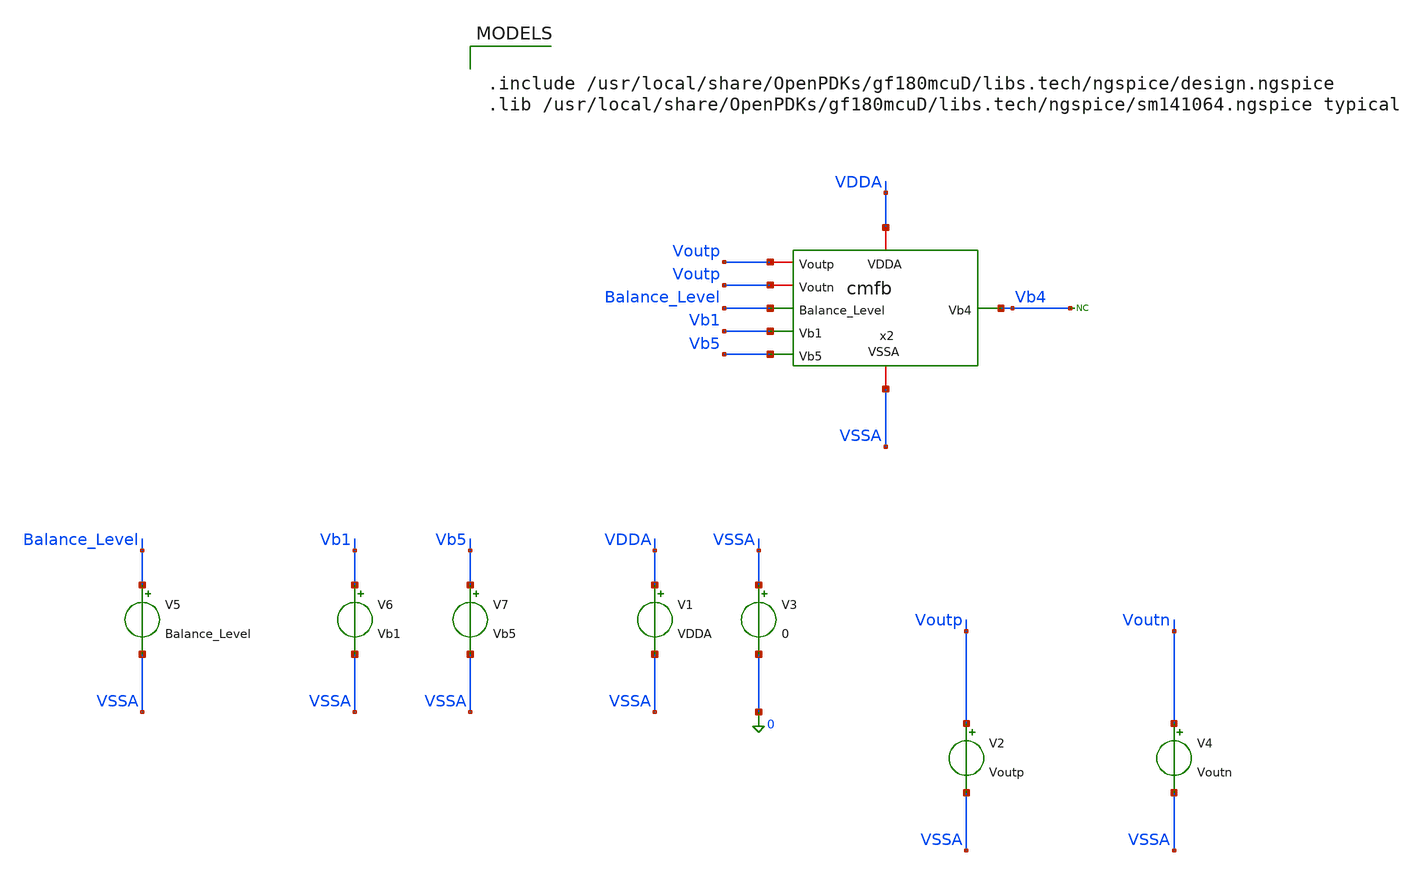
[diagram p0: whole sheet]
** sch_path: Folded_cascode/testbenches/simulation/cmfb_op_tb_batch.sch
**.subckt cmfb_op_tb_batch
x2 VDDA VSSA Voutp Voutp Balance_Level Vb1 Vb4 Vb5 cmfb
V1 VDDA VSSA VDDA
V3 VSSA 0 0
V2 Voutp VSSA Voutp
V4 Voutn VSSA Voutn
V5 Balance_Level VSSA Balance_Level
V6 Vb1 VSSA Vb1
V7 Vb5 VSSA Vb5
* noconn Vb4
**** begin user architecture code

.include /usr/local/share/OpenPDKs/gf180mcuD/libs.tech/ngspice/design.ngspice
.lib /usr/local/share/OpenPDKs/gf180mcuD/libs.tech/ngspice/sm141064.ngspice typical



.temp 27
.param VDDA = 5
.param Balance_Level = 1.3
.param Vb1 = 4.02
.param Vb5 = 0.78
.param Voutp = 2.5
.param Voutn = 2.5
.param VD = 0
.control
option sparse
set filetype=ascii
save all
save @m.x2.xm1.m0[id]
save @m.x2.xm1.m0[gm]
save @m.x2.xm1.m0[vgs]
save @m.x2.xm1.m0[vds]
save @m.x2.xm1.m0[vth]
save @m.x2.xm1.m0[gds]

save @m.x2.xm2.m0[id]
save @m.x2.xm2.m0[gm]
save @m.x2.xm2.m0[vgs]
save @m.x2.xm2.m0[vds]
save @m.x2.xm2.m0[vth]
save @m.x2.xm2.m0[gds]

save @m.x2.xm3.m0[id]
save @m.x2.xm3.m0[gm]
save @m.x2.xm3.m0[vgs]
save @m.x2.xm3.m0[vds]
save @m.x2.xm3.m0[vth]
save @m.x2.xm3.m0[gds]

save @m.x2.xm4.m0[id]
save @m.x2.xm4.m0[gm]
save @m.x2.xm4.m0[vgs]
save @m.x2.xm4.m0[vds]
save @m.x2.xm4.m0[vth]
save @m.x2.xm4.m0[gds]

save @m.x2.xm5.m0[id]
save @m.x2.xm5.m0[gm]
save @m.x2.xm5.m0[vgs]
save @m.x2.xm5.m0[vds]
save @m.x2.xm5.m0[vth]
save @m.x2.xm5.m0[gds]

save @m.x2.xm6.m0[id]
save @m.x2.xm6.m0[gm]
save @m.x2.xm6.m0[vgs]
save @m.x2.xm6.m0[vds]
save @m.x2.xm6.m0[vth]
save @m.x2.xm6.m0[gds]

save @m.x2.xm7.m0[id]
save @m.x2.xm7.m0[gm]
save @m.x2.xm7.m0[vgs]
save @m.x2.xm7.m0[vds]
save @m.x2.xm7.m0[vth]
save @m.x2.xm7.m0[gds]

save @m.x2.xm8.m0[id]
save @m.x2.xm8.m0[gm]
save @m.x2.xm8.m0[vgs]
save @m.x2.xm8.m0[vds]
save @m.x2.xm8.m0[vth]
save @m.x2.xm8.m0[gds]

save @m.x2.xm9.m0[id]
save @m.x2.xm9.m0[gm]
save @m.x2.xm9.m0[vgs]
save @m.x2.xm9.m0[vds]
save @m.x2.xm9.m0[vth]
save @m.x2.xm9.m0[gds]

op

*print v(Vb4)
*print v(x2.Vfbk) v(x2.Vdrain_M4)

write cmfb_op_tb.raw

*dc V5 0.8 1.8 0.005

*wrdata cmfb_balance_sweep.txt v(Vb4) v(x2.Vfbk) v(x2.Vdrain_M4)

.endc


**** end user architecture code
**.ends

* expanding   symbol:
*+  /home/juan/realhome/Documents/gf180/2026_chipalooza/Chipalooza_2026_INL/Folded_cascode/schematic/cmfb.sym # of pins=8
** sym_path: schematic/cmfb.sym
** sch_path: schematic/cmfb.sch
.subckt cmfb VDDA VSSA Voutp Voutn Balance_Level Vb1 Vb4 Vb5
*.iopin VDDA
*.iopin VSSA
*.ipin Vb4
*.ipin Balance_Level
*.ipin Vb1
*.ipin Vb5
*.iopin Voutp
*.iopin Voutn
XM1 net1 Vb1 VDDA VDDA pfet_05v0 L=2u W=28.6u nf=1 ad='int((nf+1)/2) * W/nf * 0.18u' as='int((nf+2)/2) * W/nf * 0.18u'
+ pd='2*int((nf+1)/2) * (W/nf + 0.18u)' ps='2*int((nf+2)/2) * (W/nf + 0.18u)' nrd='0.18u / W' nrs='0.18u / W'
+ sa=0 sb=0 sd=0 m=10
XM2 Vb4 Balance_Level net1 VDDA pfet_05v0 L=1u W=50u nf=1 ad='int((nf+1)/2) * W/nf * 0.18u' as='int((nf+2)/2) * W/nf * 0.18u'
+ pd='2*int((nf+1)/2) * (W/nf + 0.18u)' ps='2*int((nf+2)/2) * (W/nf + 0.18u)' nrd='0.18u / W' nrs='0.18u / W'
+ sa=0 sb=0 sd=0 m=1
XM3 Vdrain_M4 Vfbk net1 VDDA pfet_05v0 L=1u W=50u nf=1 ad='int((nf+1)/2) * W/nf * 0.18u' as='int((nf+2)/2) * W/nf * 0.18u'
+ pd='2*int((nf+1)/2) * (W/nf + 0.18u)' ps='2*int((nf+2)/2) * (W/nf + 0.18u)' nrd='0.18u / W' nrs='0.18u / W'
+ sa=0 sb=0 sd=0 m=1
XM4 Vdrain_M4 Vdrain_M4 VSSA VSSA nfet_05v0 L=2u W=1u nf=1 ad='int((nf+1)/2) * W/nf * 0.18u' as='int((nf+2)/2) * W/nf * 0.18u'
+ pd='2*int((nf+1)/2) * (W/nf + 0.18u)' ps='2*int((nf+2)/2) * (W/nf + 0.18u)' nrd='0.18u / W' nrs='0.18u / W'
+ sa=0 sb=0 sd=0 m=1
XM5 Vb4 Vb4 VSSA VSSA nfet_05v0 L=2u W=1u nf=1 ad='int((nf+1)/2) * W/nf * 0.18u' as='int((nf+2)/2) * W/nf * 0.18u'
+ pd='2*int((nf+1)/2) * (W/nf + 0.18u)' ps='2*int((nf+2)/2) * (W/nf + 0.18u)' nrd='0.18u / W' nrs='0.18u / W'
+ sa=0 sb=0 sd=0 m=1
XM6 VDDA Voutp net3 VSSA nfet_05v0 L=1u W=0.79u nf=1 ad='int((nf+1)/2) * W/nf * 0.18u' as='int((nf+2)/2) * W/nf * 0.18u'
+ pd='2*int((nf+1)/2) * (W/nf + 0.18u)' ps='2*int((nf+2)/2) * (W/nf + 0.18u)' nrd='0.18u / W' nrs='0.18u / W'
+ sa=0 sb=0 sd=0 m=1
XM7 VDDA Voutn net2 VSSA nfet_05v0 L=1u W=0.79u nf=1 ad='int((nf+1)/2) * W/nf * 0.18u' as='int((nf+2)/2) * W/nf * 0.18u'
+ pd='2*int((nf+1)/2) * (W/nf + 0.18u)' ps='2*int((nf+2)/2) * (W/nf + 0.18u)' nrd='0.18u / W' nrs='0.18u / W'
+ sa=0 sb=0 sd=0 m=1
R3 net3 Vfbk 100k m=1
R4 net2 Vfbk 100k m=1
XM8 net3 Vb5 VSSA VSSA nfet_05v0 L=2u W=1.86u nf=1 ad='int((nf+1)/2) * W/nf * 0.18u' as='int((nf+2)/2) * W/nf * 0.18u'
+ pd='2*int((nf+1)/2) * (W/nf + 0.18u)' ps='2*int((nf+2)/2) * (W/nf + 0.18u)' nrd='0.18u / W' nrs='0.18u / W'
+ sa=0 sb=0 sd=0 m=1
XM9 net2 Vb5 VSSA VSSA nfet_05v0 L=2u W=1.86u nf=1 ad='int((nf+1)/2) * W/nf * 0.18u' as='int((nf+2)/2) * W/nf * 0.18u'
+ pd='2*int((nf+1)/2) * (W/nf + 0.18u)' ps='2*int((nf+2)/2) * (W/nf + 0.18u)' nrd='0.18u / W' nrs='0.18u / W'
+ sa=0 sb=0 sd=0 m=1
R75 Voutn net5 25k m=1
R76 Voutp net4 25k m=1
C1 net4 net3 1p m=1
C2 net5 net2 1p m=1
.ends

.end
